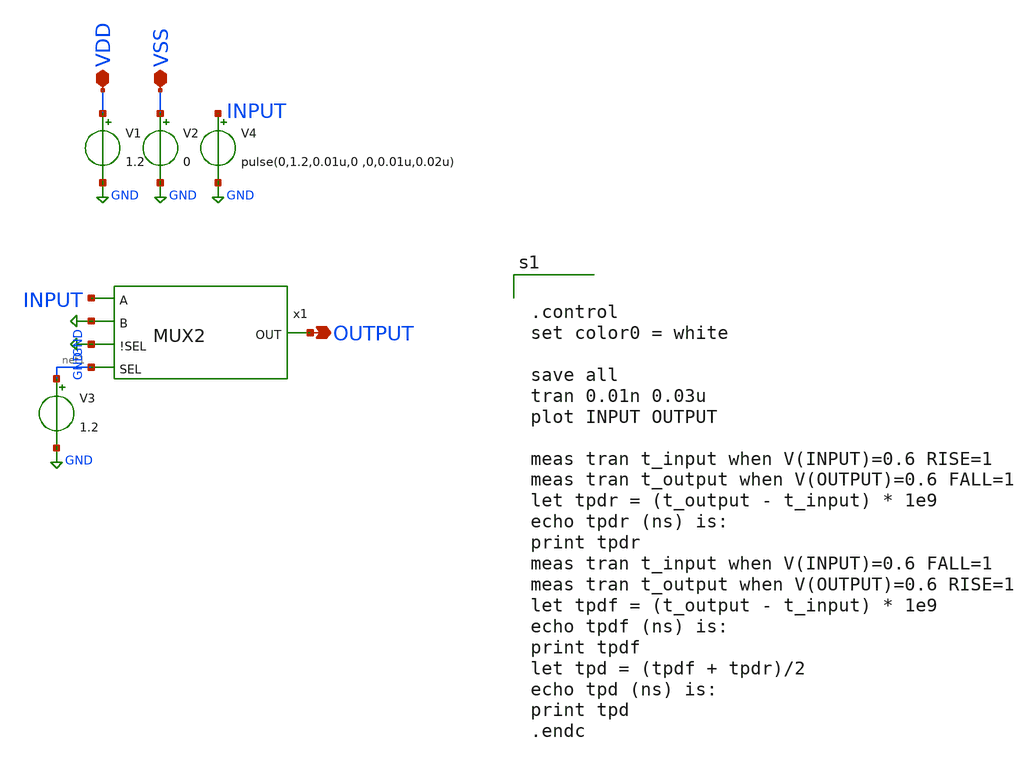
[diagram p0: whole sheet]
** sch_path: design/xschem/MUX/mux_TB.sch
**.subckt mux_TB OUTPUT VDD VSS
*.opin OUTPUT
*.iopin VDD
*.iopin VSS
V1 VDD GND 1.2
V2 VSS GND 0
V4 INPUT GND pulse(0,1.2,0.01u,0 ,0,0.01u,0.02u)
V3 net1 GND 1.2
x1 INPUT GND GND net1 OUTPUT VSS VDD MUX2
**** begin user architecture code

** opencircuitdesign pdks install
.lib $::SKYWATER_MODELS/sky130.lib.spice tt_mm




.control
set color0 = white

save all
tran 0.01n 0.03u
plot INPUT OUTPUT

meas tran t_input when V(INPUT)=0.6 RISE=1
meas tran t_output when V(OUTPUT)=0.6 FALL=1
let tpdr = (t_output - t_input) * 1e9
echo tpdr (ns) is:
print tpdr
meas tran t_input when V(INPUT)=0.6 FALL=1
meas tran t_output when V(OUTPUT)=0.6 RISE=1
let tpdf = (t_output - t_input) * 1e9
echo tpdf (ns) is:
print tpdf
let tpd = (tpdf + tpdr)/2
echo tpd (ns) is:
print tpd
.endc


**** end user architecture code
**.ends
.GLOBAL GND
.end
